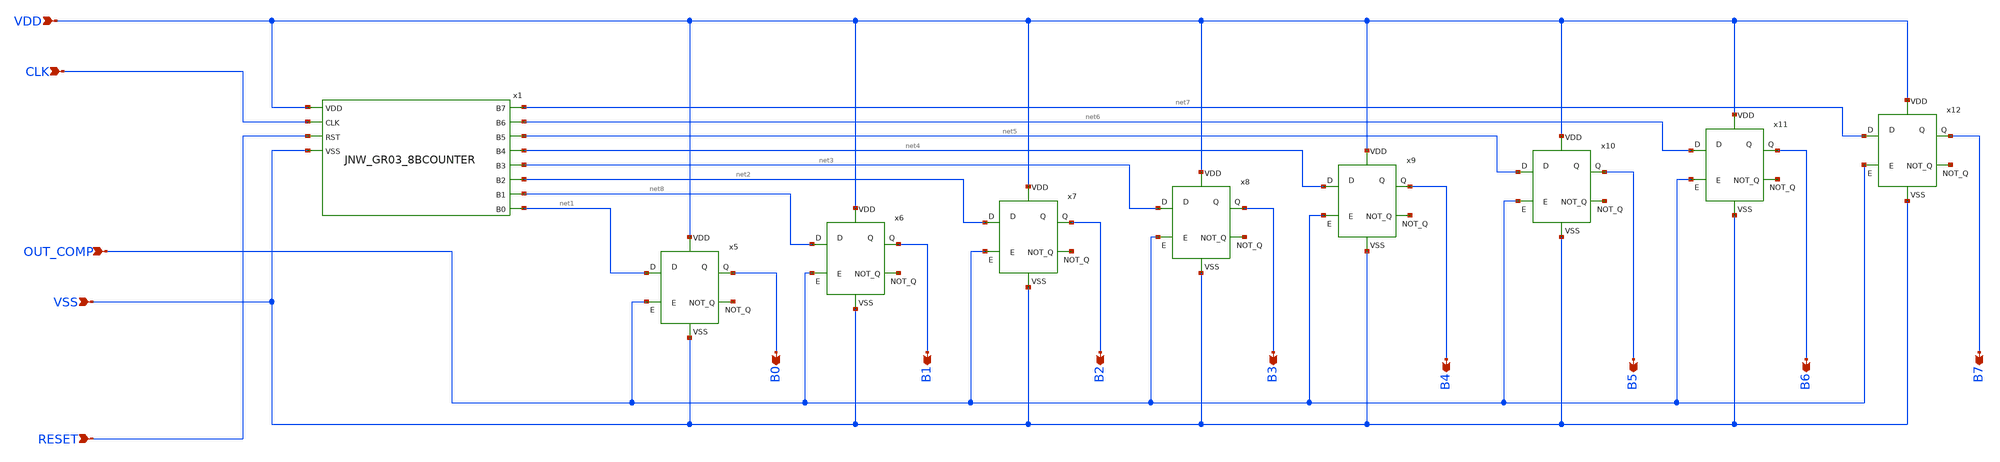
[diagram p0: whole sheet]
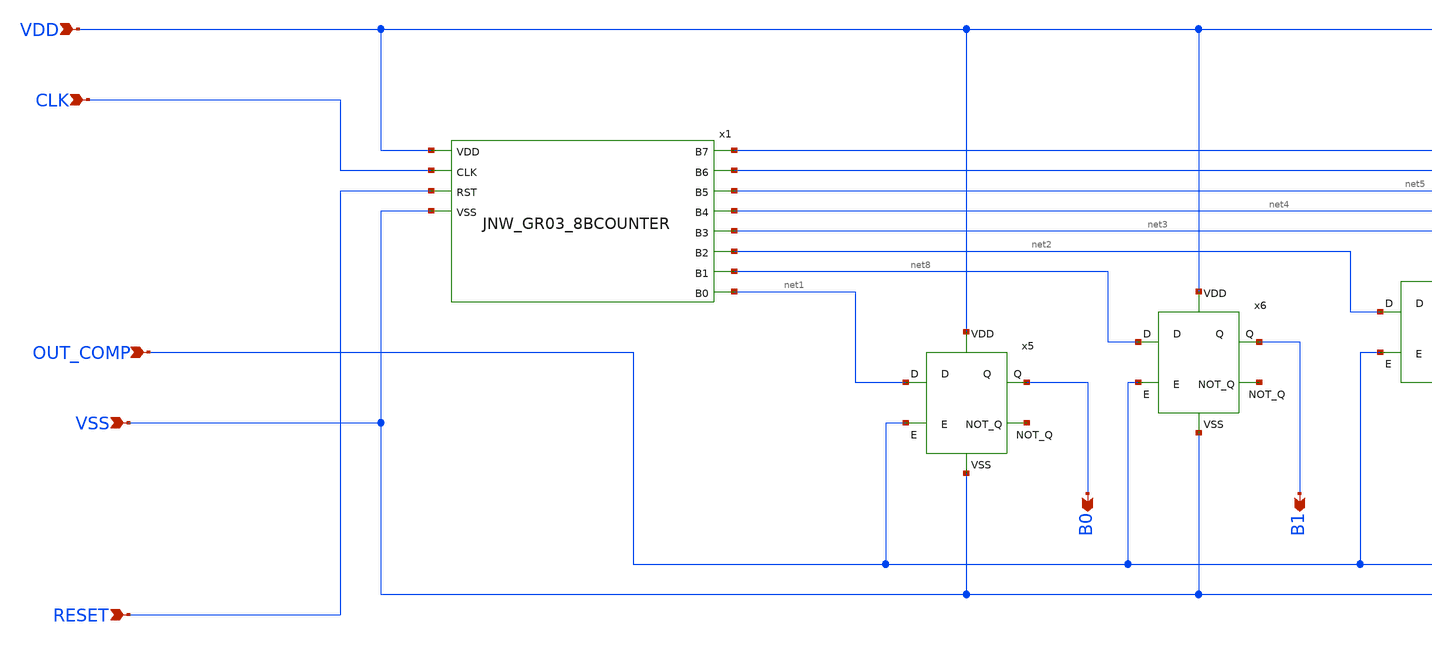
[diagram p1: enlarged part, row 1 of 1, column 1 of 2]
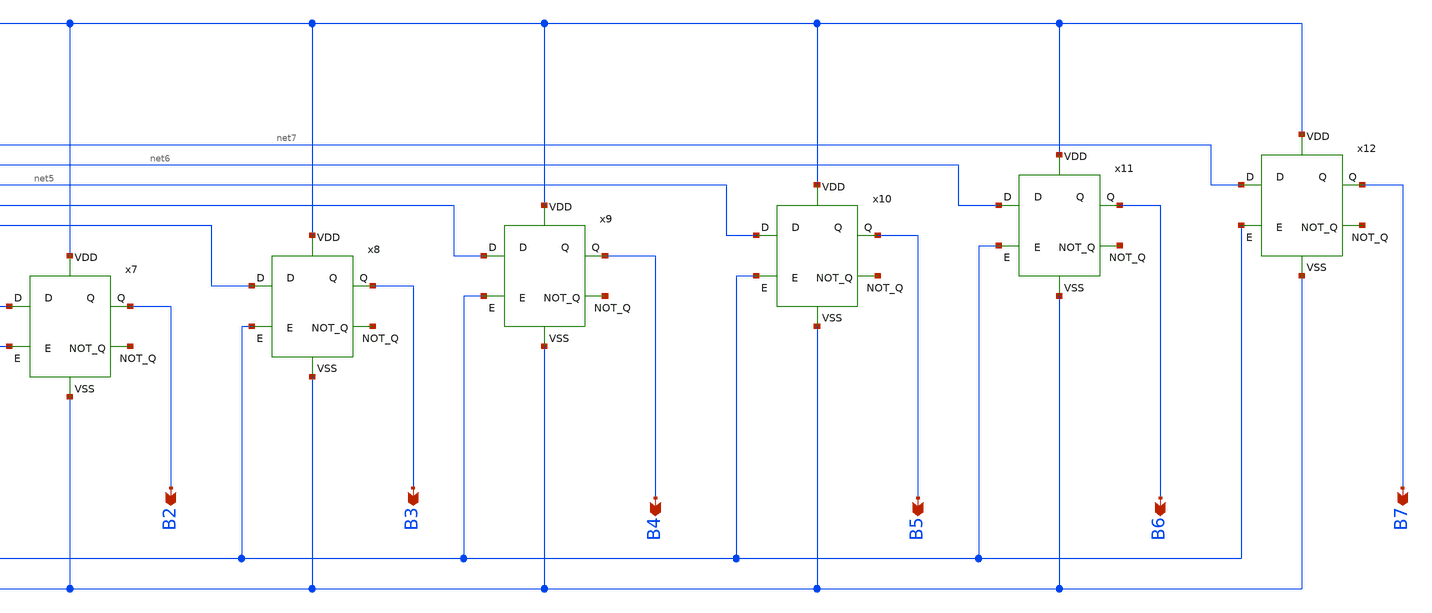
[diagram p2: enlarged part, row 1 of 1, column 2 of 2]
** sch_path: design/JNW_GR03_SKY130A/JNW_GR03_DigitalControl.sch
**.subckt JNW_GR03_DigitalControl VDD VSS OUT_COMP CLK B0 B1 B2 B3 B4 B5 B6 B7 RESET
*.ipin VDD
*.ipin VSS
*.ipin OUT_COMP
*.ipin CLK
*.opin B0
*.opin B1
*.opin B2
*.opin B3
*.opin B4
*.opin B5
*.opin B6
*.opin B7
*.ipin RESET
x1 VDD CLK RESET VSS net2 net3 net6 net5 net4 net7 net8 net1 JNW_GR03_8BCOUNTER
x5 VDD net1 B0 net9 OUT_COMP VSS JNW_GR03_DLATCH
x6 VDD net8 B1 net10 OUT_COMP VSS JNW_GR03_DLATCH
x7 VDD net2 B2 net11 OUT_COMP VSS JNW_GR03_DLATCH
x8 VDD net3 B3 net12 OUT_COMP VSS JNW_GR03_DLATCH
x9 VDD net4 B4 net13 OUT_COMP VSS JNW_GR03_DLATCH
x10 VDD net5 B5 net14 OUT_COMP VSS JNW_GR03_DLATCH
x11 VDD net6 B6 net15 OUT_COMP VSS JNW_GR03_DLATCH
x12 VDD net7 B7 net16 OUT_COMP VSS JNW_GR03_DLATCH
**.ends
.end
